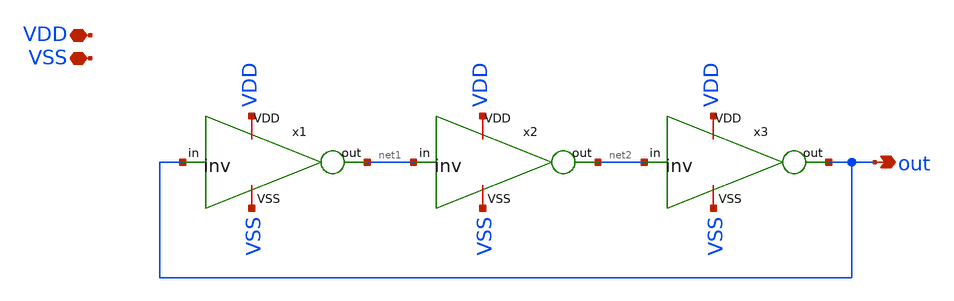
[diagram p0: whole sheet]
** sch_path: xsch/ip/ringOsc/ringOsc.sch
**.subckt ringOsc out VDD VSS
*.opin out
*.iopin VDD
*.iopin VSS
x1 VDD out net1 VSS inv
x2 VDD net1 net2 VSS inv
x3 VDD net2 out VSS inv
**.ends

* expanding   symbol:  ip/inv/inv.sym # of pins=4
** sym_path: xsch/ip/inv/inv.sym
** sch_path: xsch/ip/inv/inv.sch
.subckt inv VDD in out VSS
*.ipin in
*.opin out
*.iopin VDD
*.iopin VSS
XM2 out in VSS VSS sky130_fd_pr__nfet_01v8 L=0.15 W=1 nf=1 ad='int((1 + 1)/2) * 1 / 1 * 0.29' as='int((1 + 2)/2) * 1 / 1 * 0.29'
+ pd='2*int((1 + 1)/2) * (1 / 1 + 0.29)' ps='2*int((1 + 2)/2) * (1 / 1 + 0.29)' nrd='0.29 / 1 ' nrs='0.29 / 1 '
+ sa=0 sb=0 sd=0 mult=1 m=1
XM11 out in VDD VDD sky130_fd_pr__pfet_01v8 L=0.15 W=1 nf=1 ad='int((nf+1)/2) * W/nf * 0.29' as='int((nf+2)/2) * W/nf * 0.29'
+ pd='2*int((nf+1)/2) * (W/nf + 0.29)' ps='2*int((nf+2)/2) * (W/nf + 0.29)' nrd='0.29 / W' nrs='0.29 / W'
+ sa=0 sb=0 sd=0 mult=1 m=1
.ends

.end
